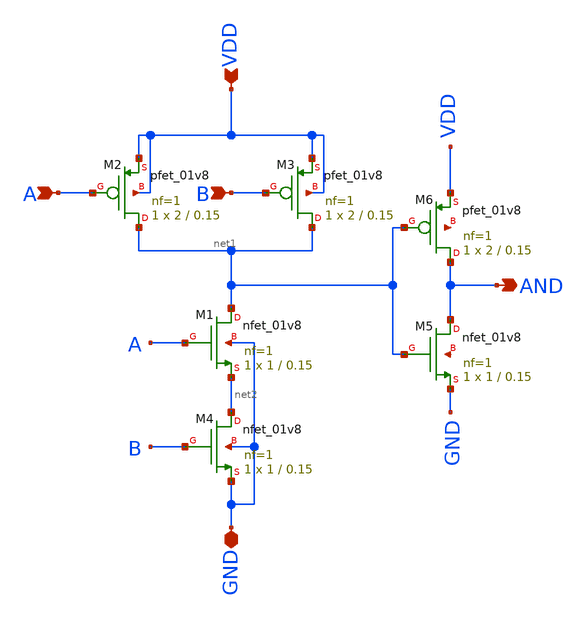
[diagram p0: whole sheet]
** sch_path: skywater_stuff/untitled-6.sch
**.subckt untitled-6 A B AND GND VDD
*.ipin A
*.ipin B
*.opin AND
*.iopin GND
*.ipin VDD
XM1 net1 A net2 GND sky130_fd_pr__nfet_01v8 L=0.15 W=1 nf=1 ad='int((nf+1)/2) * W/nf * 0.29' as='int((nf+2)/2) * W/nf * 0.29'
+ pd='2*int((nf+1)/2) * (W/nf + 0.29)' ps='2*int((nf+2)/2) * (W/nf + 0.29)' nrd='0.29 / W' nrs='0.29 / W'
+ sa=0 sb=0 sd=0 mult=1 m=1
XM2 net1 A VDD VDD sky130_fd_pr__pfet_01v8 L=0.15 W=2 nf=1 ad='int((nf+1)/2) * W/nf * 0.29' as='int((nf+2)/2) * W/nf * 0.29'
+ pd='2*int((nf+1)/2) * (W/nf + 0.29)' ps='2*int((nf+2)/2) * (W/nf + 0.29)' nrd='0.29 / W' nrs='0.29 / W'
+ sa=0 sb=0 sd=0 mult=1 m=1
XM3 net1 B VDD VDD sky130_fd_pr__pfet_01v8 L=0.15 W=2 nf=1 ad='int((nf+1)/2) * W/nf * 0.29' as='int((nf+2)/2) * W/nf * 0.29'
+ pd='2*int((nf+1)/2) * (W/nf + 0.29)' ps='2*int((nf+2)/2) * (W/nf + 0.29)' nrd='0.29 / W' nrs='0.29 / W'
+ sa=0 sb=0 sd=0 mult=1 m=1
XM4 net2 B GND GND sky130_fd_pr__nfet_01v8 L=0.15 W=1 nf=1 ad='int((nf+1)/2) * W/nf * 0.29' as='int((nf+2)/2) * W/nf * 0.29'
+ pd='2*int((nf+1)/2) * (W/nf + 0.29)' ps='2*int((nf+2)/2) * (W/nf + 0.29)' nrd='0.29 / W' nrs='0.29 / W'
+ sa=0 sb=0 sd=0 mult=1 m=1
XM5 AND net1 GND net3 sky130_fd_pr__nfet_01v8 L=0.15 W=1 nf=1 ad='int((nf+1)/2) * W/nf * 0.29' as='int((nf+2)/2) * W/nf * 0.29'
+ pd='2*int((nf+1)/2) * (W/nf + 0.29)' ps='2*int((nf+2)/2) * (W/nf + 0.29)' nrd='0.29 / W' nrs='0.29 / W'
+ sa=0 sb=0 sd=0 mult=1 m=1
XM6 AND net1 VDD net4 sky130_fd_pr__pfet_01v8 L=0.15 W=2 nf=1 ad='int((nf+1)/2) * W/nf * 0.29' as='int((nf+2)/2) * W/nf * 0.29'
+ pd='2*int((nf+1)/2) * (W/nf + 0.29)' ps='2*int((nf+2)/2) * (W/nf + 0.29)' nrd='0.29 / W' nrs='0.29 / W'
+ sa=0 sb=0 sd=0 mult=1 m=1
**.ends
.end
